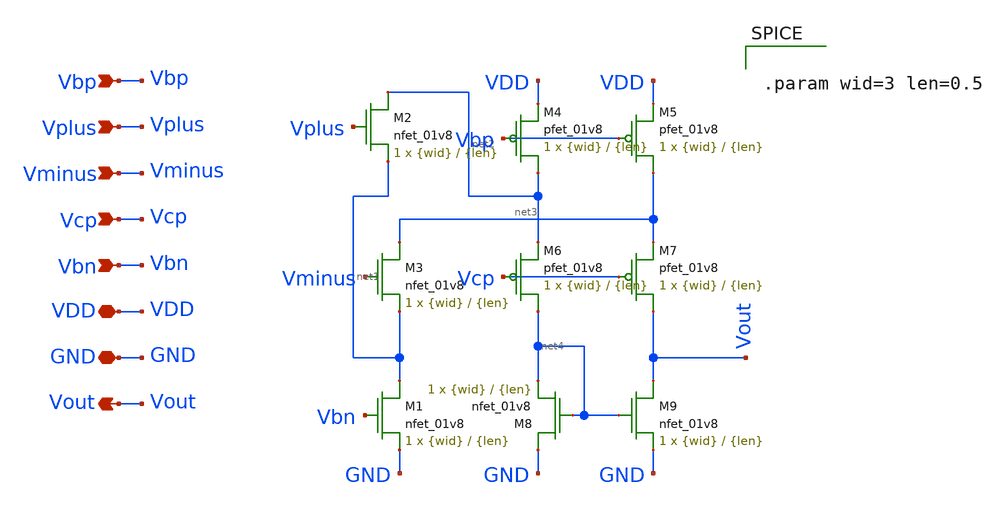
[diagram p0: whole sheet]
** sch_path: final/LDS/cascoded_opamp_LDS.sch
**.subckt cascoded_opamp_LDS Vbp Vplus Vminus Vcp Vbn VDD GND Vout
*.ipin Vbp
*.ipin Vplus
*.ipin Vminus
*.ipin Vcp
*.ipin Vbn
*.iopin VDD
*.iopin GND
*.opin Vout
XM1 net1 Vbn GND GND sky130_fd_pr__nfet_01v8 L={len} W={wid} nf=1 ad='int((nf+1)/2) * W/nf * 0.29' as='int((nf+2)/2) * W/nf * 0.29'
+ pd='2*int((nf+1)/2) * (W/nf + 0.29)' ps='2*int((nf+2)/2) * (W/nf + 0.29)' nrd='0.29 / W' nrs='0.29 / W'
+ sa=0 sb=0 sd=0 mult=1 m=1
XM2 net2 Vplus net1 GND sky130_fd_pr__nfet_01v8 L={len} W={wid} nf=1 ad='int((nf+1)/2) * W/nf * 0.29'
+ as='int((nf+2)/2) * W/nf * 0.29' pd='2*int((nf+1)/2) * (W/nf + 0.29)' ps='2*int((nf+2)/2) * (W/nf + 0.29)'
+ nrd='0.29 / W' nrs='0.29 / W' sa=0 sb=0 sd=0 mult=1 m=1
XM3 net3 Vminus net1 GND sky130_fd_pr__nfet_01v8 L={len} W={wid} nf=1 ad='int((nf+1)/2) * W/nf * 0.29'
+ as='int((nf+2)/2) * W/nf * 0.29' pd='2*int((nf+1)/2) * (W/nf + 0.29)' ps='2*int((nf+2)/2) * (W/nf + 0.29)'
+ nrd='0.29 / W' nrs='0.29 / W' sa=0 sb=0 sd=0 mult=1 m=1
XM4 net2 Vbp VDD VDD sky130_fd_pr__pfet_01v8 L={len} W={wid} nf=1 ad='int((nf+1)/2) * W/nf * 0.29' as='int((nf+2)/2) * W/nf * 0.29'
+ pd='2*int((nf+1)/2) * (W/nf + 0.29)' ps='2*int((nf+2)/2) * (W/nf + 0.29)' nrd='0.29 / W' nrs='0.29 / W'
+ sa=0 sb=0 sd=0 mult=1 m=1
XM5 net3 Vbp VDD VDD sky130_fd_pr__pfet_01v8 L={len} W={wid} nf=1 ad='int((nf+1)/2) * W/nf * 0.29' as='int((nf+2)/2) * W/nf * 0.29'
+ pd='2*int((nf+1)/2) * (W/nf + 0.29)' ps='2*int((nf+2)/2) * (W/nf + 0.29)' nrd='0.29 / W' nrs='0.29 / W'
+ sa=0 sb=0 sd=0 mult=1 m=1
XM6 net4 Vcp net2 VDD sky130_fd_pr__pfet_01v8 L={len} W={wid} nf=1 ad='int((nf+1)/2) * W/nf * 0.29' as='int((nf+2)/2) * W/nf * 0.29'
+ pd='2*int((nf+1)/2) * (W/nf + 0.29)' ps='2*int((nf+2)/2) * (W/nf + 0.29)' nrd='0.29 / W' nrs='0.29 / W'
+ sa=0 sb=0 sd=0 mult=1 m=1
XM7 Vout Vcp net3 VDD sky130_fd_pr__pfet_01v8 L={len} W={wid} nf=1 ad='int((nf+1)/2) * W/nf * 0.29' as='int((nf+2)/2) * W/nf * 0.29'
+ pd='2*int((nf+1)/2) * (W/nf + 0.29)' ps='2*int((nf+2)/2) * (W/nf + 0.29)' nrd='0.29 / W' nrs='0.29 / W'
+ sa=0 sb=0 sd=0 mult=1 m=1
XM8 GND net4 net4 GND sky130_fd_pr__nfet_01v8 L={len} W={wid} nf=1 ad='int((nf+1)/2) * W/nf * 0.29' as='int((nf+2)/2) * W/nf * 0.29'
+ pd='2*int((nf+1)/2) * (W/nf + 0.29)' ps='2*int((nf+2)/2) * (W/nf + 0.29)' nrd='0.29 / W' nrs='0.29 / W'
+ sa=0 sb=0 sd=0 mult=1 m=1
XM9 Vout net4 GND GND sky130_fd_pr__nfet_01v8 L={len} W={wid} nf=1 ad='int((nf+1)/2) * W/nf * 0.29' as='int((nf+2)/2) * W/nf * 0.29'
+ pd='2*int((nf+1)/2) * (W/nf + 0.29)' ps='2*int((nf+2)/2) * (W/nf + 0.29)' nrd='0.29 / W' nrs='0.29 / W'
+ sa=0 sb=0 sd=0 mult=1 m=1
**** begin user architecture code


.param wid=3 len=0.5


**** end user architecture code
**.ends
.end
